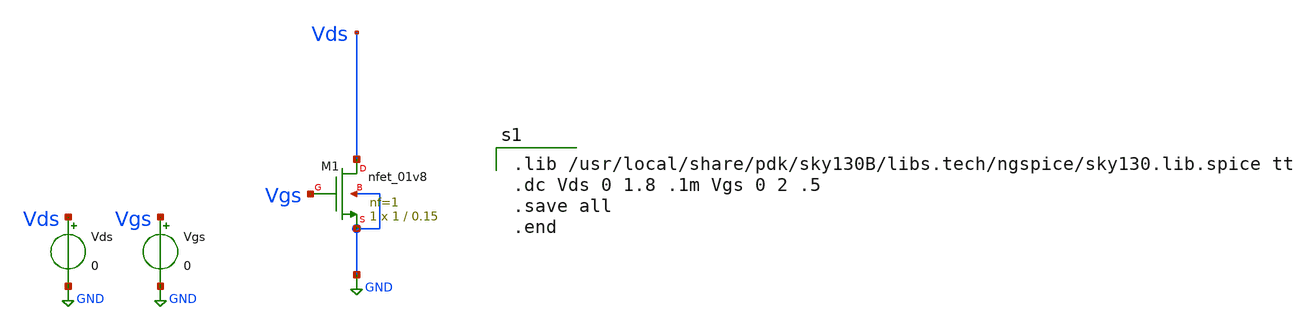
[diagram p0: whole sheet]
** sch_path: nmos_char.sch
**.subckt nmos_char
Vds Vds GND 0
Vgs Vgs GND 0
XM1 Vds Vgs GND GND sky130_fd_pr__nfet_01v8 L=0.15 W=1 nf=1 ad='int((nf+1)/2) * W/nf * 0.29' as='int((nf+2)/2) * W/nf * 0.29'
+ pd='2*int((nf+1)/2) * (W/nf + 0.29)' ps='2*int((nf+2)/2) * (W/nf + 0.29)' nrd='0.29 / W' nrs='0.29 / W'
+ sa=0 sb=0 sd=0 mult=1 m=1
**** begin user architecture code

.lib /usr/local/share/pdk/sky130B/libs.tech/ngspice/sky130.lib.spice tt
.dc Vds 0 1.8 .1m Vgs 0 2 .5
.save all
.end

**** end user architecture code
**.ends
.GLOBAL GND
.end
